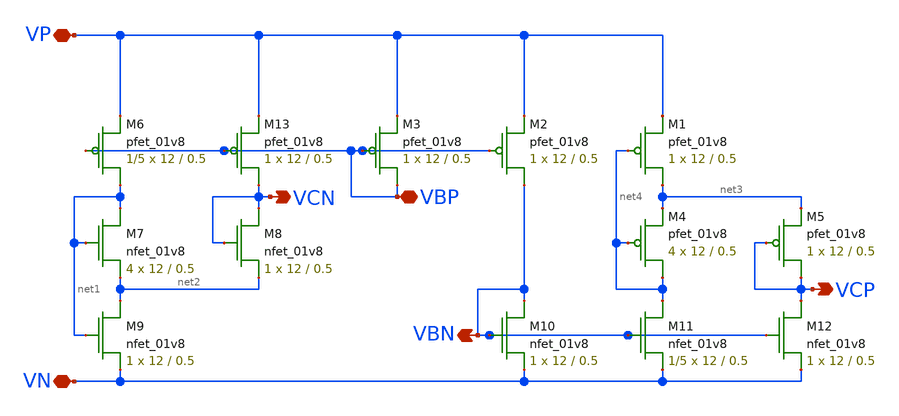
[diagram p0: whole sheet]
** sch_path: mp3/schematics/bias_generator.sch
**.subckt bias_generator VP VN VCN VBN VCP VBP
*.iopin VP
*.iopin VN
*.opin VCN
*.opin VBN
*.opin VCP
*.iopin VBP
XM4 net4 net4 net3 VDD sky130_fd_pr__pfet_01v8 L=0.5 W=12 nf=1 ad='int((nf+1)/2) * W/nf * 0.29' as='int((nf+2)/2) * W/nf * 0.29'
+ pd='2*int((nf+1)/2) * (W/nf + 0.29)' ps='2*int((nf+2)/2) * (W/nf + 0.29)' nrd='0.29 / W' nrs='0.29 / W'
+ sa=0 sb=0 sd=0 mult=4 m=4
XM5 VCP VCP net3 VDD sky130_fd_pr__pfet_01v8 L=0.5 W=12 nf=1 ad='int((nf+1)/2) * W/nf * 0.29' as='int((nf+2)/2) * W/nf * 0.29'
+ pd='2*int((nf+1)/2) * (W/nf + 0.29)' ps='2*int((nf+2)/2) * (W/nf + 0.29)' nrd='0.29 / W' nrs='0.29 / W'
+ sa=0 sb=0 sd=0 mult=1 m=1
XM1 net3 net4 VP VDD sky130_fd_pr__pfet_01v8 L=0.5 W=12 nf=1 ad='int((nf+1)/2) * W/nf * 0.29' as='int((nf+2)/2) * W/nf * 0.29'
+ pd='2*int((nf+1)/2) * (W/nf + 0.29)' ps='2*int((nf+2)/2) * (W/nf + 0.29)' nrd='0.29 / W' nrs='0.29 / W'
+ sa=0 sb=0 sd=0 mult=1 m=1
XM6 net1 VBP VP VDD sky130_fd_pr__pfet_01v8 L=0.5 W=12 nf=1 ad='int((nf+1)/2) * W/nf * 0.29' as='int((nf+2)/2) * W/nf * 0.29'
+ pd='2*int((nf+1)/2) * (W/nf + 0.29)' ps='2*int((nf+2)/2) * (W/nf + 0.29)' nrd='0.29 / W' nrs='0.29 / W'
+ sa=0 sb=0 sd=0 mult=1/5 m=1/5
XM11 net4 VBN VN GND sky130_fd_pr__nfet_01v8 L=0.5 W=12 nf=1 ad='int((nf+1)/2) * W/nf * 0.29' as='int((nf+2)/2) * W/nf * 0.29'
+ pd='2*int((nf+1)/2) * (W/nf + 0.29)' ps='2*int((nf+2)/2) * (W/nf + 0.29)' nrd='0.29 / W' nrs='0.29 / W'
+ sa=0 sb=0 sd=0 mult=1/5 m=1/5
XM12 VCP VBN VN GND sky130_fd_pr__nfet_01v8 L=0.5 W=12 nf=1 ad='int((nf+1)/2) * W/nf * 0.29' as='int((nf+2)/2) * W/nf * 0.29'
+ pd='2*int((nf+1)/2) * (W/nf + 0.29)' ps='2*int((nf+2)/2) * (W/nf + 0.29)' nrd='0.29 / W' nrs='0.29 / W'
+ sa=0 sb=0 sd=0 mult=1 m=1
XM9 net2 net1 VN GND sky130_fd_pr__nfet_01v8 L=0.5 W=12 nf=1 ad='int((nf+1)/2) * W/nf * 0.29' as='int((nf+2)/2) * W/nf * 0.29'
+ pd='2*int((nf+1)/2) * (W/nf + 0.29)' ps='2*int((nf+2)/2) * (W/nf + 0.29)' nrd='0.29 / W' nrs='0.29 / W'
+ sa=0 sb=0 sd=0 mult=1 m=1
XM8 VCN VCN net2 GND sky130_fd_pr__nfet_01v8 L=0.5 W=12 nf=1 ad='int((nf+1)/2) * W/nf * 0.29' as='int((nf+2)/2) * W/nf * 0.29'
+ pd='2*int((nf+1)/2) * (W/nf + 0.29)' ps='2*int((nf+2)/2) * (W/nf + 0.29)' nrd='0.29 / W' nrs='0.29 / W'
+ sa=0 sb=0 sd=0 mult=1 m=1
XM7 net1 net1 net2 GND sky130_fd_pr__nfet_01v8 L=0.5 W=12 nf=1 ad='int((nf+1)/2) * W/nf * 0.29' as='int((nf+2)/2) * W/nf * 0.29'
+ pd='2*int((nf+1)/2) * (W/nf + 0.29)' ps='2*int((nf+2)/2) * (W/nf + 0.29)' nrd='0.29 / W' nrs='0.29 / W'
+ sa=0 sb=0 sd=0 mult=4 m=4
XM2 VBN VBP VP VDD sky130_fd_pr__pfet_01v8 L=0.5 W=12 nf=1 ad='int((nf+1)/2) * W/nf * 0.29' as='int((nf+2)/2) * W/nf * 0.29'
+ pd='2*int((nf+1)/2) * (W/nf + 0.29)' ps='2*int((nf+2)/2) * (W/nf + 0.29)' nrd='0.29 / W' nrs='0.29 / W'
+ sa=0 sb=0 sd=0 mult=1 m=1
XM13 VCN VBP VP VDD sky130_fd_pr__pfet_01v8 L=0.5 W=12 nf=1 ad='int((nf+1)/2) * W/nf * 0.29' as='int((nf+2)/2) * W/nf * 0.29'
+ pd='2*int((nf+1)/2) * (W/nf + 0.29)' ps='2*int((nf+2)/2) * (W/nf + 0.29)' nrd='0.29 / W' nrs='0.29 / W'
+ sa=0 sb=0 sd=0 mult=1 m=1
XM3 VBP VBP VP VDD sky130_fd_pr__pfet_01v8 L=0.5 W=12 nf=1 ad='int((nf+1)/2) * W/nf * 0.29' as='int((nf+2)/2) * W/nf * 0.29'
+ pd='2*int((nf+1)/2) * (W/nf + 0.29)' ps='2*int((nf+2)/2) * (W/nf + 0.29)' nrd='0.29 / W' nrs='0.29 / W'
+ sa=0 sb=0 sd=0 mult=1 m=1
XM10 VBN VBN VN GND sky130_fd_pr__nfet_01v8 L=0.5 W=12 nf=1 ad='int((nf+1)/2) * W/nf * 0.29' as='int((nf+2)/2) * W/nf * 0.29'
+ pd='2*int((nf+1)/2) * (W/nf + 0.29)' ps='2*int((nf+2)/2) * (W/nf + 0.29)' nrd='0.29 / W' nrs='0.29 / W'
+ sa=0 sb=0 sd=0 mult=1 m=1
**.ends
.end
